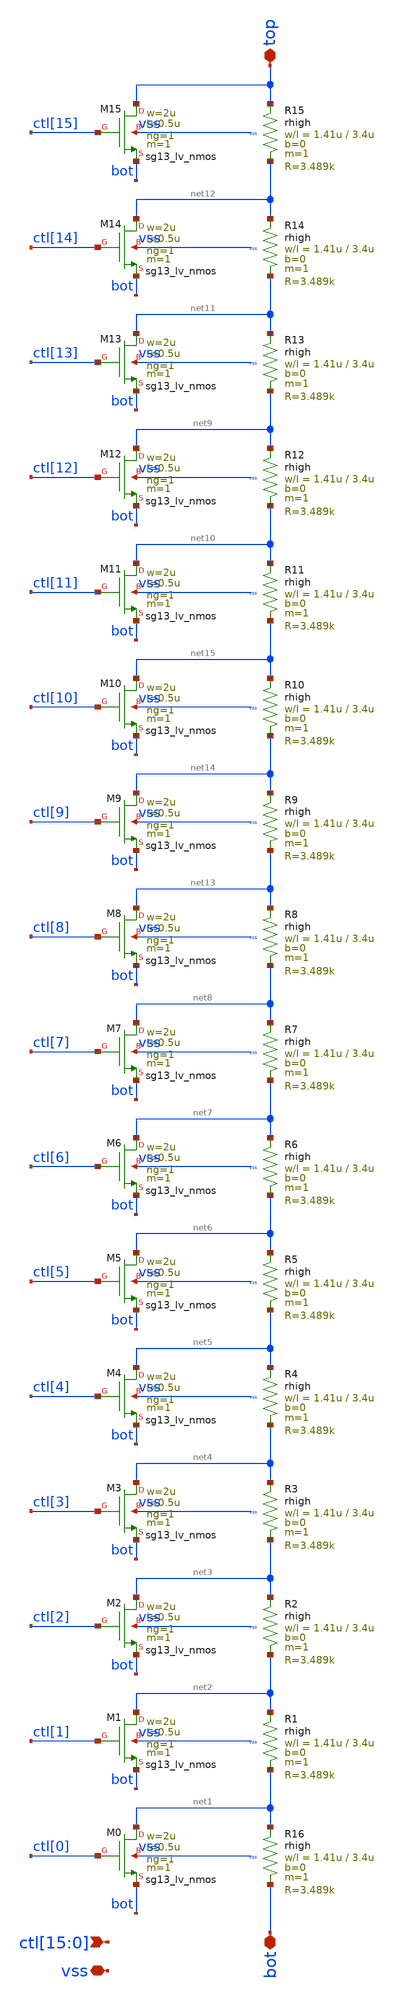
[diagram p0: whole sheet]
** sch_path: xschem/bandgap_orig/bg_trim.sch
**.subckt bg_trim vss
*+ ctl[15],ctl[14],ctl[13],ctl[12],ctl[11],ctl[10],ctl[9],ctl[8],ctl[7],ctl[6],ctl[5],ctl[4],ctl[3],ctl[2],ctl[1],ctl[0] bot top
*.iopin vss
*.ipin
*+ ctl[15],ctl[14],ctl[13],ctl[12],ctl[11],ctl[10],ctl[9],ctl[8],ctl[7],ctl[6],ctl[5],ctl[4],ctl[3],ctl[2],ctl[1],ctl[0]
*.iopin bot
*.iopin top
XM0 net1 ctl[0] bot vss sg13_lv_nmos w=2u l=0.5u ng=1 m=1 mm_ok=1
XM1 net2 ctl[1] bot vss sg13_lv_nmos w=2u l=0.5u ng=1 m=1 mm_ok=1
XM2 net3 ctl[2] bot vss sg13_lv_nmos w=2u l=0.5u ng=1 m=1 mm_ok=1
XM3 net4 ctl[3] bot vss sg13_lv_nmos w=2u l=0.5u ng=1 m=1 mm_ok=1
XM4 net5 ctl[4] bot vss sg13_lv_nmos w=2u l=0.5u ng=1 m=1 mm_ok=1
XM5 net6 ctl[5] bot vss sg13_lv_nmos w=2u l=0.5u ng=1 m=1 mm_ok=1
XM6 net7 ctl[6] bot vss sg13_lv_nmos w=2u l=0.5u ng=1 m=1 mm_ok=1
XM7 net8 ctl[7] bot vss sg13_lv_nmos w=2u l=0.5u ng=1 m=1 mm_ok=1
XM12 net9 ctl[12] bot vss sg13_lv_nmos w=2u l=0.5u ng=1 m=1 mm_ok=1
XM13 net11 ctl[13] bot vss sg13_lv_nmos w=2u l=0.5u ng=1 m=1 mm_ok=1
XM14 net12 ctl[14] bot vss sg13_lv_nmos w=2u l=0.5u ng=1 m=1 mm_ok=1
XM15 top ctl[15] bot vss sg13_lv_nmos w=2u l=0.5u ng=1 m=1 mm_ok=1
XM8 net13 ctl[8] bot vss sg13_lv_nmos w=2u l=0.5u ng=1 m=1 mm_ok=1
XM9 net14 ctl[9] bot vss sg13_lv_nmos w=2u l=0.5u ng=1 m=1 mm_ok=1
XM10 net15 ctl[10] bot vss sg13_lv_nmos w=2u l=0.5u ng=1 m=1 mm_ok=1
XM11 net10 ctl[11] bot vss sg13_lv_nmos w=2u l=0.5u ng=1 m=1 mm_ok=1
XR15 top net12 vss rhigh w=1.41u l=3.4u m=1 b=0 mm_ok=1
XR1 net2 net1 vss rhigh w=1.41u l=3.4u m=1 b=0 mm_ok=1
XR16 net1 bot vss rhigh w=1.41u l=3.4u m=1 b=0 mm_ok=1
XR2 net3 net2 vss rhigh w=1.41u l=3.4u m=1 b=0 mm_ok=1
XR3 net4 net3 vss rhigh w=1.41u l=3.4u m=1 b=0 mm_ok=1
XR4 net5 net4 vss rhigh w=1.41u l=3.4u m=1 b=0 mm_ok=1
XR5 net6 net5 vss rhigh w=1.41u l=3.4u m=1 b=0 mm_ok=1
XR6 net7 net6 vss rhigh w=1.41u l=3.4u m=1 b=0 mm_ok=1
XR7 net8 net7 vss rhigh w=1.41u l=3.4u m=1 b=0 mm_ok=1
XR8 net13 net8 vss rhigh w=1.41u l=3.4u m=1 b=0 mm_ok=1
XR9 net14 net13 vss rhigh w=1.41u l=3.4u m=1 b=0 mm_ok=1
XR10 net15 net14 vss rhigh w=1.41u l=3.4u m=1 b=0 mm_ok=1
XR11 net10 net15 vss rhigh w=1.41u l=3.4u m=1 b=0 mm_ok=1
XR12 net9 net10 vss rhigh w=1.41u l=3.4u m=1 b=0 mm_ok=1
XR13 net11 net9 vss rhigh w=1.41u l=3.4u m=1 b=0 mm_ok=1
XR14 net12 net11 vss rhigh w=1.41u l=3.4u m=1 b=0 mm_ok=1
**.ends
.end
